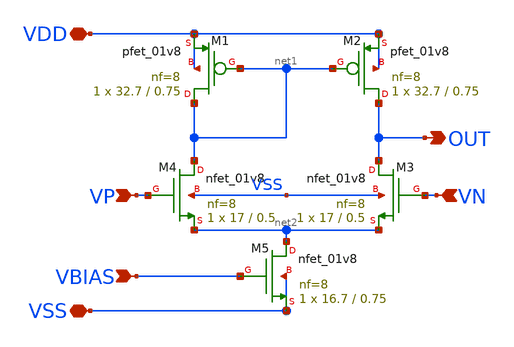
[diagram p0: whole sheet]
** sch_path: LDO_UVLO_Design/LDO2/5t-ota.sch
**.subckt 5t-ota OUT VDD VSS VP VN VBIAS
*.opin OUT
*.iopin VDD
*.iopin VSS
*.ipin VP
*.ipin VN
*.ipin VBIAS
XM1 net1 net1 VDD VDD sky130_fd_pr__pfet_01v8 L=0.75 W=32.7 nf=8 ad='int((nf+1)/2) * W/nf * 0.29' as='int((nf+2)/2) * W/nf * 0.29'
+ pd='2*int((nf+1)/2) * (W/nf + 0.29)' ps='2*int((nf+2)/2) * (W/nf + 0.29)' nrd='0.29 / W' nrs='0.29 / W'
+ sa=0 sb=0 sd=0 mult=1 m=1
XM2 OUT net1 VDD VDD sky130_fd_pr__pfet_01v8 L=0.75 W=32.7 nf=8 ad='int((nf+1)/2) * W/nf * 0.29' as='int((nf+2)/2) * W/nf * 0.29'
+ pd='2*int((nf+1)/2) * (W/nf + 0.29)' ps='2*int((nf+2)/2) * (W/nf + 0.29)' nrd='0.29 / W' nrs='0.29 / W'
+ sa=0 sb=0 sd=0 mult=1 m=1
XM3 OUT VN net2 VSS sky130_fd_pr__nfet_01v8 L=0.5 W=17 nf=8 ad='int((nf+1)/2) * W/nf * 0.29' as='int((nf+2)/2) * W/nf * 0.29'
+ pd='2*int((nf+1)/2) * (W/nf + 0.29)' ps='2*int((nf+2)/2) * (W/nf + 0.29)' nrd='0.29 / W' nrs='0.29 / W'
+ sa=0 sb=0 sd=0 mult=1 m=1
XM4 net1 VP net2 VSS sky130_fd_pr__nfet_01v8 L=0.5 W=17 nf=8 ad='int((nf+1)/2) * W/nf * 0.29' as='int((nf+2)/2) * W/nf * 0.29'
+ pd='2*int((nf+1)/2) * (W/nf + 0.29)' ps='2*int((nf+2)/2) * (W/nf + 0.29)' nrd='0.29 / W' nrs='0.29 / W'
+ sa=0 sb=0 sd=0 mult=1 m=1
XM5 net2 VBIAS VSS VSS sky130_fd_pr__nfet_01v8 L=0.75 W=16.7 nf=8 ad='int((nf+1)/2) * W/nf * 0.29' as='int((nf+2)/2) * W/nf * 0.29'
+ pd='2*int((nf+1)/2) * (W/nf + 0.29)' ps='2*int((nf+2)/2) * (W/nf + 0.29)' nrd='0.29 / W' nrs='0.29 / W'
+ sa=0 sb=0 sd=0 mult=1 m=1
**.ends
.end
